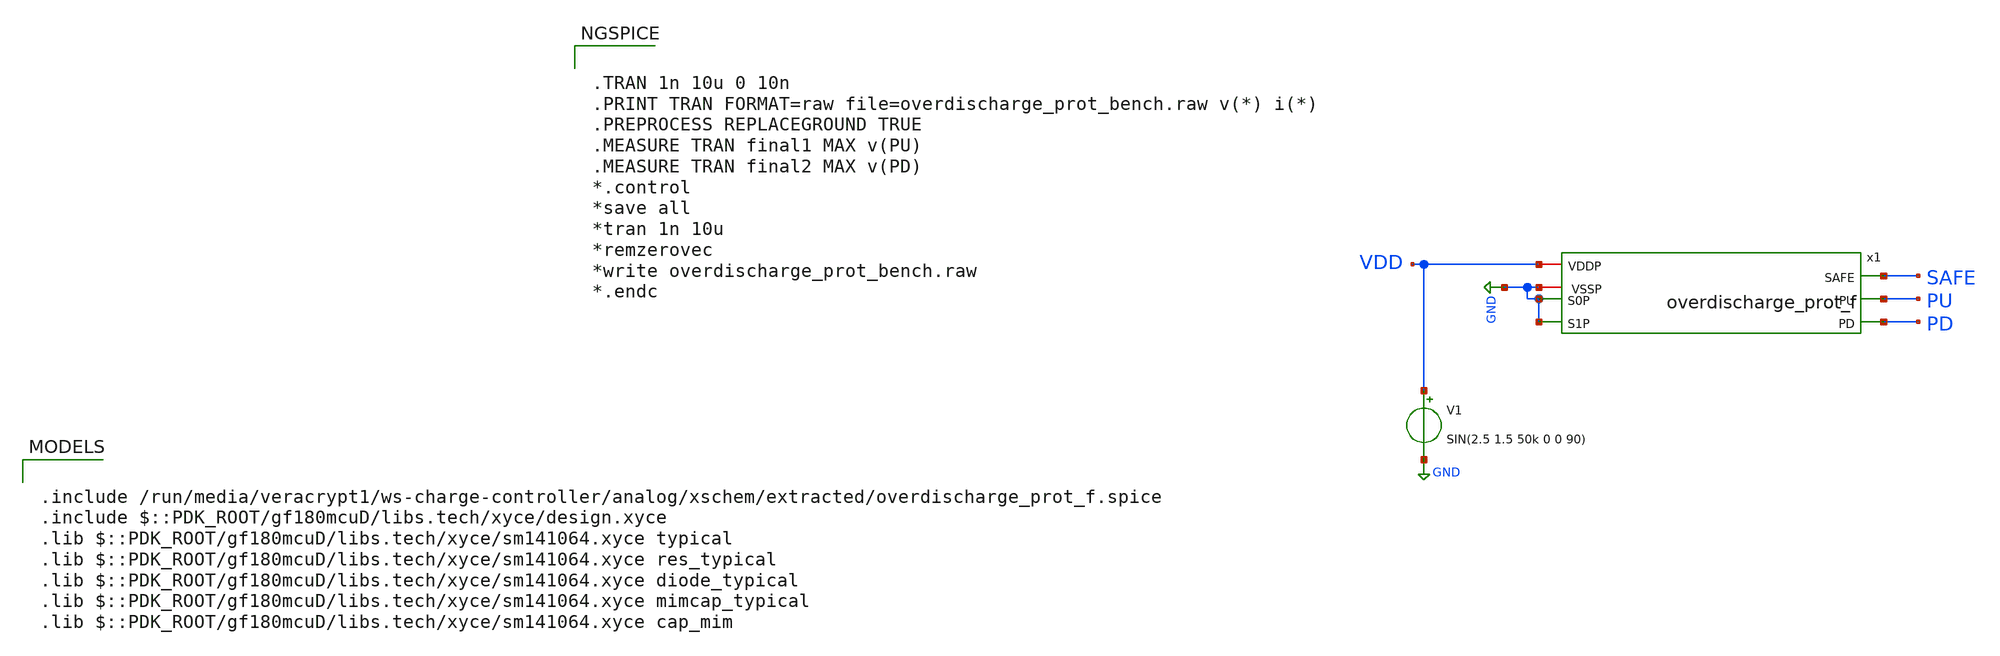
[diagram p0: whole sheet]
** sch_path: analog/xschem/overdischarge_prot_bench.sch
**.subckt overdischarge_prot_bench
V1 VDD GND SIN(2.5 1.5 50k 0 0 90)
x1 VDD GND GND GND SAFE PD PU overdischarge_prot_f
**** begin user architecture code


.TRAN 1n 10u 0 10n
.PRINT TRAN FORMAT=raw file=overdischarge_prot_bench.raw v(*) i(*)
.PREPROCESS REPLACEGROUND TRUE
.MEASURE TRAN final1 MAX v(PU)
.MEASURE TRAN final2 MAX v(PD)
*.control
*save all
*tran 1n 10u
*remzerovec
*write overdischarge_prot_bench.raw
*.endc



.include /run/media/veracrypt1/ws-charge-controller/analog/xschem/extracted/overdischarge_prot_f.spice
.include $::PDK_ROOT/gf180mcuD/libs.tech/xyce/design.xyce
.lib $::PDK_ROOT/gf180mcuD/libs.tech/xyce/sm141064.xyce typical
.lib $::PDK_ROOT/gf180mcuD/libs.tech/xyce/sm141064.xyce res_typical
.lib $::PDK_ROOT/gf180mcuD/libs.tech/xyce/sm141064.xyce diode_typical
.lib $::PDK_ROOT/gf180mcuD/libs.tech/xyce/sm141064.xyce mimcap_typical
.lib $::PDK_ROOT/gf180mcuD/libs.tech/xyce/sm141064.xyce cap_mim

**** end user architecture code
**.ends
.GLOBAL GND
.end
